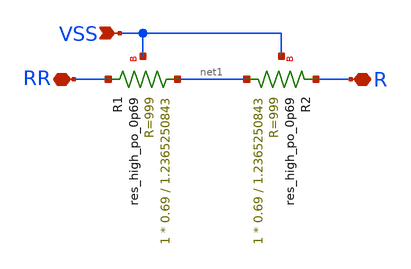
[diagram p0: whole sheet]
** sch_path: xschem/untitled-1.sch
**.subckt untitled-1 R RR VSS
*.iopin R
*.iopin RR
*.ipin VSS
XR1 net1 RR VSS sky130_fd_pr__res_high_po_0p69 L=1.2365250843 mult=1 m=1
XR2 net1 R VSS sky130_fd_pr__res_high_po_0p69 L=1.2365250843 mult=1 m=1
**.ends
.end
